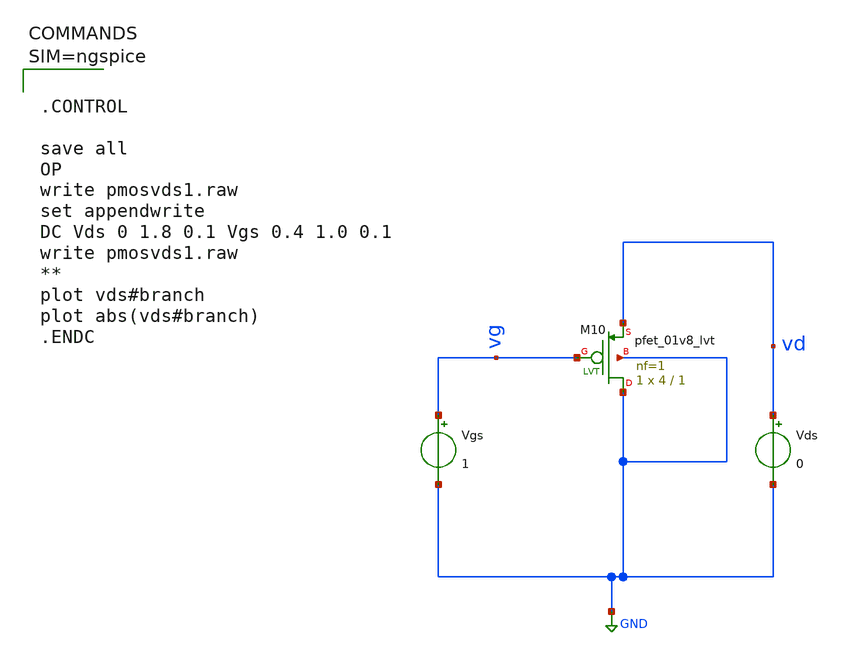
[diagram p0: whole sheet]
** sch_path: work/xschem/pmosvds1.sch
**.subckt pmosvds1
Vgs vg GND 1
Vds vd GND 0
XM10 GND vg vd GND sky130_fd_pr__pfet_01v8_lvt L=1 W=4 nf=1 ad='int((1 + 1)/2) * 4 / 1 * 0.29' as='int((1 + 2)/2) * 4 / 1 * 0.29'
+ pd='2*int((1 + 1)/2) * (4 / 1 + 0.29)' ps='2*int((1 + 2)/2) * (4 / 1 + 0.29)' nrd='0.29 / 4 ' nrs='0.29 / 4 '
+ sa=0 sb=0 sd=0 mult=1 m=1
**** begin user architecture code



.CONTROL

save all
OP
write pmosvds1.raw
set appendwrite
DC Vds 0 1.8 0.1 Vgs 0.4 1.0 0.1
write pmosvds1.raw
**
plot vds#branch
plot abs(vds#branch)
.ENDC




** opencircuitdesign pdks install
.lib $::SKYWATER_MODELS/sky130.lib.spice tt

**** end user architecture code
**.ends
.GLOBAL GND
.end
